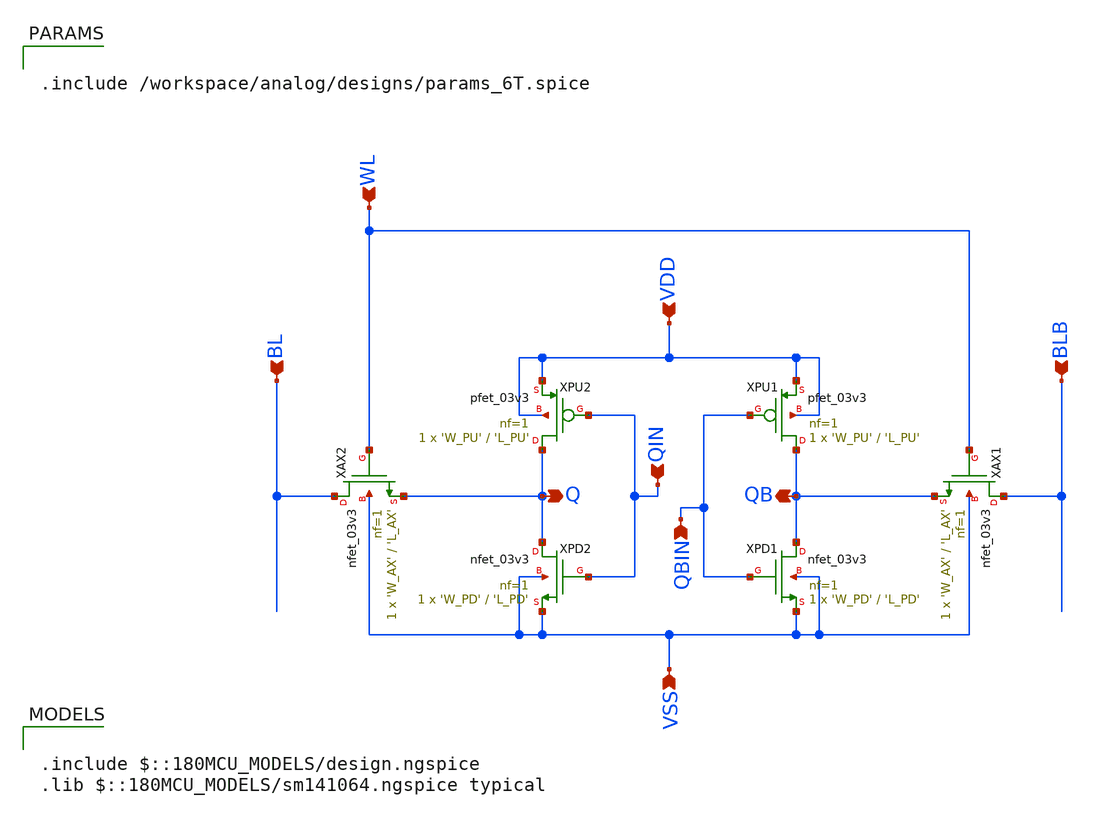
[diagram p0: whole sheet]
** sch_path: analog/designs/6T_03v3.sch
**.subckt 6T_03v3 VSS VDD WL BL BLB QBIN QIN Q QB
*.ipin VSS
*.ipin VDD
*.ipin WL
*.ipin BL
*.ipin BLB
*.ipin QBIN
*.ipin QIN
*.opin Q
*.opin QB
XPD1 QB QBIN VSS VSS nfet_03v3 L='L_PD' W='W_PD' nf=1 ad='int((nf+1)/2) * W/nf * 0.18u' as='int((nf+2)/2) * W/nf * 0.18u'
+ pd='2*int((nf+1)/2) * (W/nf + 0.18u)' ps='2*int((nf+2)/2) * (W/nf + 0.18u)' nrd='0.18u / W' nrs='0.18u / W'
+ sa=0 sb=0 sd=0 m=1
XPU1 QB QBIN VDD VDD pfet_03v3 L='L_PU' W='W_PU' nf=1 ad='int((nf+1)/2) * W/nf * 0.18u' as='int((nf+2)/2) * W/nf * 0.18u'
+ pd='2*int((nf+1)/2) * (W/nf + 0.18u)' ps='2*int((nf+2)/2) * (W/nf + 0.18u)' nrd='0.18u / W' nrs='0.18u / W'
+ sa=0 sb=0 sd=0 m=1
XAX1 BLB WL QB VSS nfet_03v3 L='L_AX' W='W_AX' nf=1 ad='int((nf+1)/2) * W/nf * 0.18u' as='int((nf+2)/2) * W/nf * 0.18u'
+ pd='2*int((nf+1)/2) * (W/nf + 0.18u)' ps='2*int((nf+2)/2) * (W/nf + 0.18u)' nrd='0.18u / W' nrs='0.18u / W'
+ sa=0 sb=0 sd=0 m=1
XPU2 Q QIN VDD VDD pfet_03v3 L='L_PU' W='W_PU' nf=1 ad='int((nf+1)/2) * W/nf * 0.18u' as='int((nf+2)/2) * W/nf * 0.18u'
+ pd='2*int((nf+1)/2) * (W/nf + 0.18u)' ps='2*int((nf+2)/2) * (W/nf + 0.18u)' nrd='0.18u / W' nrs='0.18u / W'
+ sa=0 sb=0 sd=0 m=1
XPD2 Q QIN VSS VSS nfet_03v3 L='L_PD' W='W_PD' nf=1 ad='int((nf+1)/2) * W/nf * 0.18u' as='int((nf+2)/2) * W/nf * 0.18u'
+ pd='2*int((nf+1)/2) * (W/nf + 0.18u)' ps='2*int((nf+2)/2) * (W/nf + 0.18u)' nrd='0.18u / W' nrs='0.18u / W'
+ sa=0 sb=0 sd=0 m=1
XAX2 BL WL Q VSS nfet_03v3 L='L_AX' W='W_AX' nf=1 ad='int((nf+1)/2) * W/nf * 0.18u' as='int((nf+2)/2) * W/nf * 0.18u'
+ pd='2*int((nf+1)/2) * (W/nf + 0.18u)' ps='2*int((nf+2)/2) * (W/nf + 0.18u)' nrd='0.18u / W' nrs='0.18u / W'
+ sa=0 sb=0 sd=0 m=1
**** begin user architecture code

.include /workspace/analog/designs/params_6T.spice


.include $::180MCU_MODELS/design.ngspice
.lib $::180MCU_MODELS/sm141064.ngspice typical

**** end user architecture code
**.ends
.end
